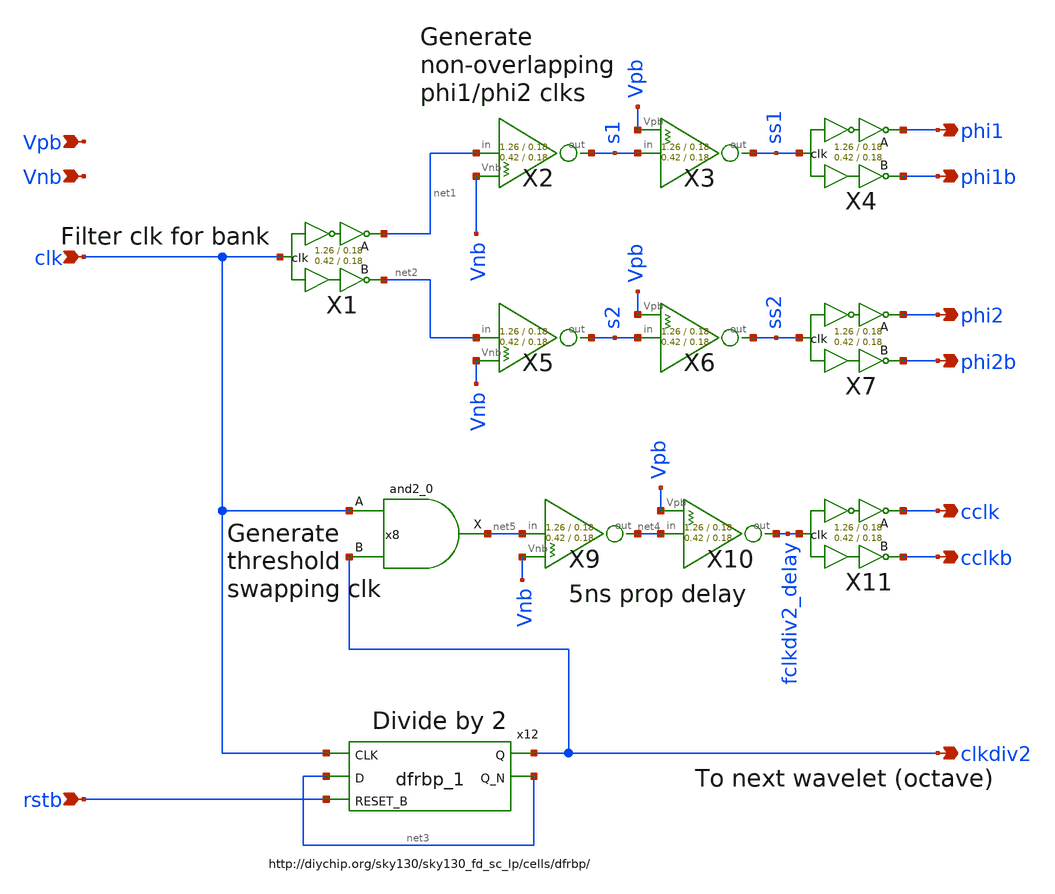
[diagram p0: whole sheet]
** sch_path: xschem/clkgen/filter_clkgen_and.sch
**.subckt filter_clkgen_and clk rstb phi1 phi1b phi2 phi2b cclk cclkb clkdiv2 Vpb Vnb
*.ipin clk
*.ipin rstb
*.opin phi1
*.opin phi1b
*.opin phi2
*.opin phi2b
*.opin cclk
*.opin cclkb
*.opin clkdiv2
*.ipin Vpb
*.ipin Vnb
X3 s1 ss1 Vpb inv_weak_pullup Wpmos=1.26 Lpmos=0.18 Wnmos=0.42 Lnmos=0.18
X2 net1 s1 Vnb inv_weak_pulldown Wpmos=1.26 Lpmos=0.18 Wnmos=0.42 Lnmos=0.18
x12 clk net3 rstb gnd gnd vdd vdd clkdiv2 net3 sky130_fd_sc_lp__dfrbp_1
x8 clk clkdiv2 gnd gnd vdd vdd net5 sky130_fd_sc_lp__and2_0
X1 clk net1 net2 comp_clks Wpmos=1.26 Lpmos=0.18 Wnmos=0.42 Lnmos=0.18
X4 ss1 phi1 phi1b comp_clks Wpmos=1.26 Lpmos=0.18 Wnmos=0.42 Lnmos=0.18
X7 ss2 phi2 phi2b comp_clks Wpmos=1.26 Lpmos=0.18 Wnmos=0.42 Lnmos=0.18
X11 fclkdiv2_delay cclk cclkb comp_clks Wpmos=1.26 Lpmos=0.18 Wnmos=0.42 Lnmos=0.18
X5 net2 s2 Vnb inv_weak_pulldown Wpmos=1.26 Lpmos=0.18 Wnmos=0.42 Lnmos=0.18
X6 s2 ss2 Vpb inv_weak_pullup Wpmos=1.26 Lpmos=0.18 Wnmos=0.42 Lnmos=0.18
X9 net5 net4 Vnb inv_weak_pulldown Wpmos=1.26 Lpmos=0.18 Wnmos=0.42 Lnmos=0.18
X10 net4 fclkdiv2_delay Vpb inv_weak_pullup Wpmos=1.26 Lpmos=0.18 Wnmos=0.42 Lnmos=0.18
**.ends
.end
